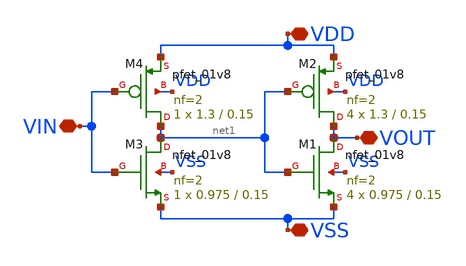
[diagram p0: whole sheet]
** sch_path: xschem/xschem_BGR_Top/Sigma_Delta/Buffer_for_Clock/Buffer_for_Clock.sch
**.subckt Buffer_for_Clock VIN VDD VSS VOUT
*.iopin VIN
*.iopin VDD
*.iopin VSS
*.iopin VOUT
XM2 VOUT net1 VDD VDD sky130_fd_pr__pfet_01v8 L=0.15 W=1.3 nf=2 ad='int((nf+1)/2) * W/nf * 0.29' as='int((nf+2)/2) * W/nf * 0.29'
+ pd='2*int((nf+1)/2) * (W/nf + 0.29)' ps='2*int((nf+2)/2) * (W/nf + 0.29)' nrd='0.29 / W' nrs='0.29 / W'
+ sa=0 sb=0 sd=0 mult=4 m=4
XM4 net1 VIN VDD VDD sky130_fd_pr__pfet_01v8 L=0.15 W=1.3 nf=2 ad='int((nf+1)/2) * W/nf * 0.29' as='int((nf+2)/2) * W/nf * 0.29'
+ pd='2*int((nf+1)/2) * (W/nf + 0.29)' ps='2*int((nf+2)/2) * (W/nf + 0.29)' nrd='0.29 / W' nrs='0.29 / W'
+ sa=0 sb=0 sd=0 mult=1 m=1
XM3 net1 VIN VSS VSS sky130_fd_pr__nfet_01v8 L=0.15 W=0.975 nf=2 ad='int((nf+1)/2) * W/nf * 0.29' as='int((nf+2)/2) * W/nf * 0.29'
+ pd='2*int((nf+1)/2) * (W/nf + 0.29)' ps='2*int((nf+2)/2) * (W/nf + 0.29)' nrd='0.29 / W' nrs='0.29 / W'
+ sa=0 sb=0 sd=0 mult=1 m=1
XM1 VOUT net1 VSS VSS sky130_fd_pr__nfet_01v8 L=0.15 W=0.975 nf=2 ad='int((nf+1)/2) * W/nf * 0.29' as='int((nf+2)/2) * W/nf * 0.29'
+ pd='2*int((nf+1)/2) * (W/nf + 0.29)' ps='2*int((nf+2)/2) * (W/nf + 0.29)' nrd='0.29 / W' nrs='0.29 / W'
+ sa=0 sb=0 sd=0 mult=4 m=4
**** begin user architecture code

** opencircuitdesign pdks install
.lib $::SKYWATER_MODELS/sky130.lib.spice tt


**** end user architecture code
**.ends
.end
